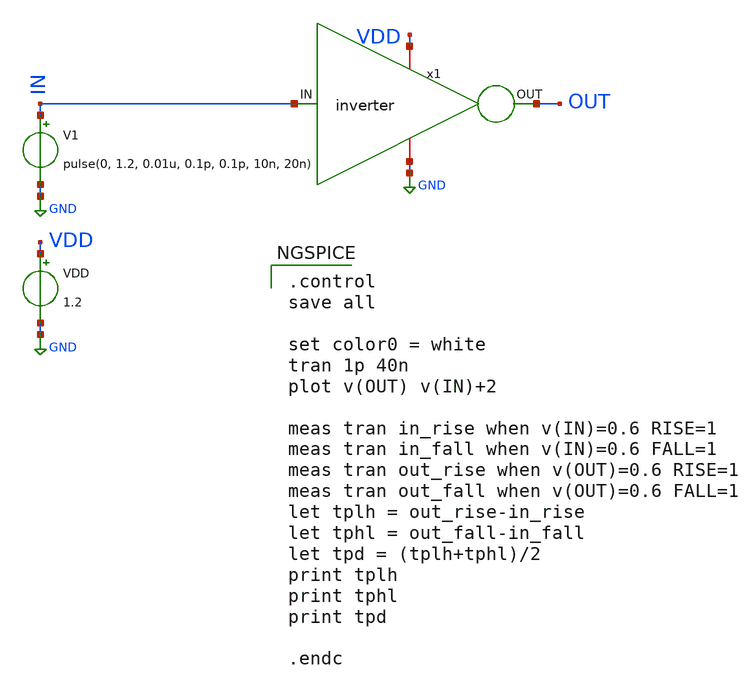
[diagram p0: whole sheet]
** sch_path: design/INV/xschem/inverter_tb.sch
**.subckt inverter_tb
x1 VDD OUT IN GND inverter
VDD VDD GND 1.2
V1 IN GND pulse(0, 1.2, 0.01u, 0.1p, 0.1p, 10n, 20n)
**** begin user architecture code

** opencircuitdesign pdks install
.lib $::SKYWATER_MODELS/sky130.lib.spice tt_mm



.control
save all

set color0 = white
tran 1p 40n
plot v(OUT) v(IN)+2

meas tran in_rise when v(IN)=0.6 RISE=1
meas tran in_fall when v(IN)=0.6 FALL=1
meas tran out_rise when v(OUT)=0.6 RISE=1
meas tran out_fall when v(OUT)=0.6 FALL=1
let tplh = out_rise-in_rise
let tphl = out_fall-in_fall
let tpd = (tplh+tphl)/2
print tplh
print tphl
print tpd

.endc

**** end user architecture code
**.ends

* expanding   symbol:  inverter.sym # of pins=4
** sym_path: design/ALU/inverter.sym
** sch_path: design/ALU/inverter.sch
.subckt inverter VDD OUT IN VSS
*.ipin IN
*.iopin VDD
*.opin OUT
*.iopin VSS
XM2 OUT IN VDD VDD sky130_fd_pr__pfet_01v8 L=0.15 W=0.9 nf=1 ad='int((nf+1)/2) * W/nf * 0.29' as='int((nf+2)/2) * W/nf * 0.29'
+ pd='2*int((nf+1)/2) * (W/nf + 0.29)' ps='2*int((nf+2)/2) * (W/nf + 0.29)' nrd='0.29 / W' nrs='0.29 / W'
+ sa=0 sb=0 sd=0 mult=1 m=1
XM1 OUT IN VSS VSS sky130_fd_pr__nfet_01v8 L=0.15 W=0.42 nf=1 ad='int((1 + 1)/2) * 0.42 / 1 * 0.29' as='int((1 + 2)/2) * 0.42 / 1 * 0.29'
+ pd='2*int((1 + 1)/2) * (0.42 / 1 + 0.29)' ps='2*int((1 + 2)/2) * (0.42 / 1 + 0.29)' nrd='0.29 / 0.42 '
+ nrs='0.29 / 0.42 ' sa=0 sb=0 sd=0 mult=1 m=1
.ends

.GLOBAL GND
.end
